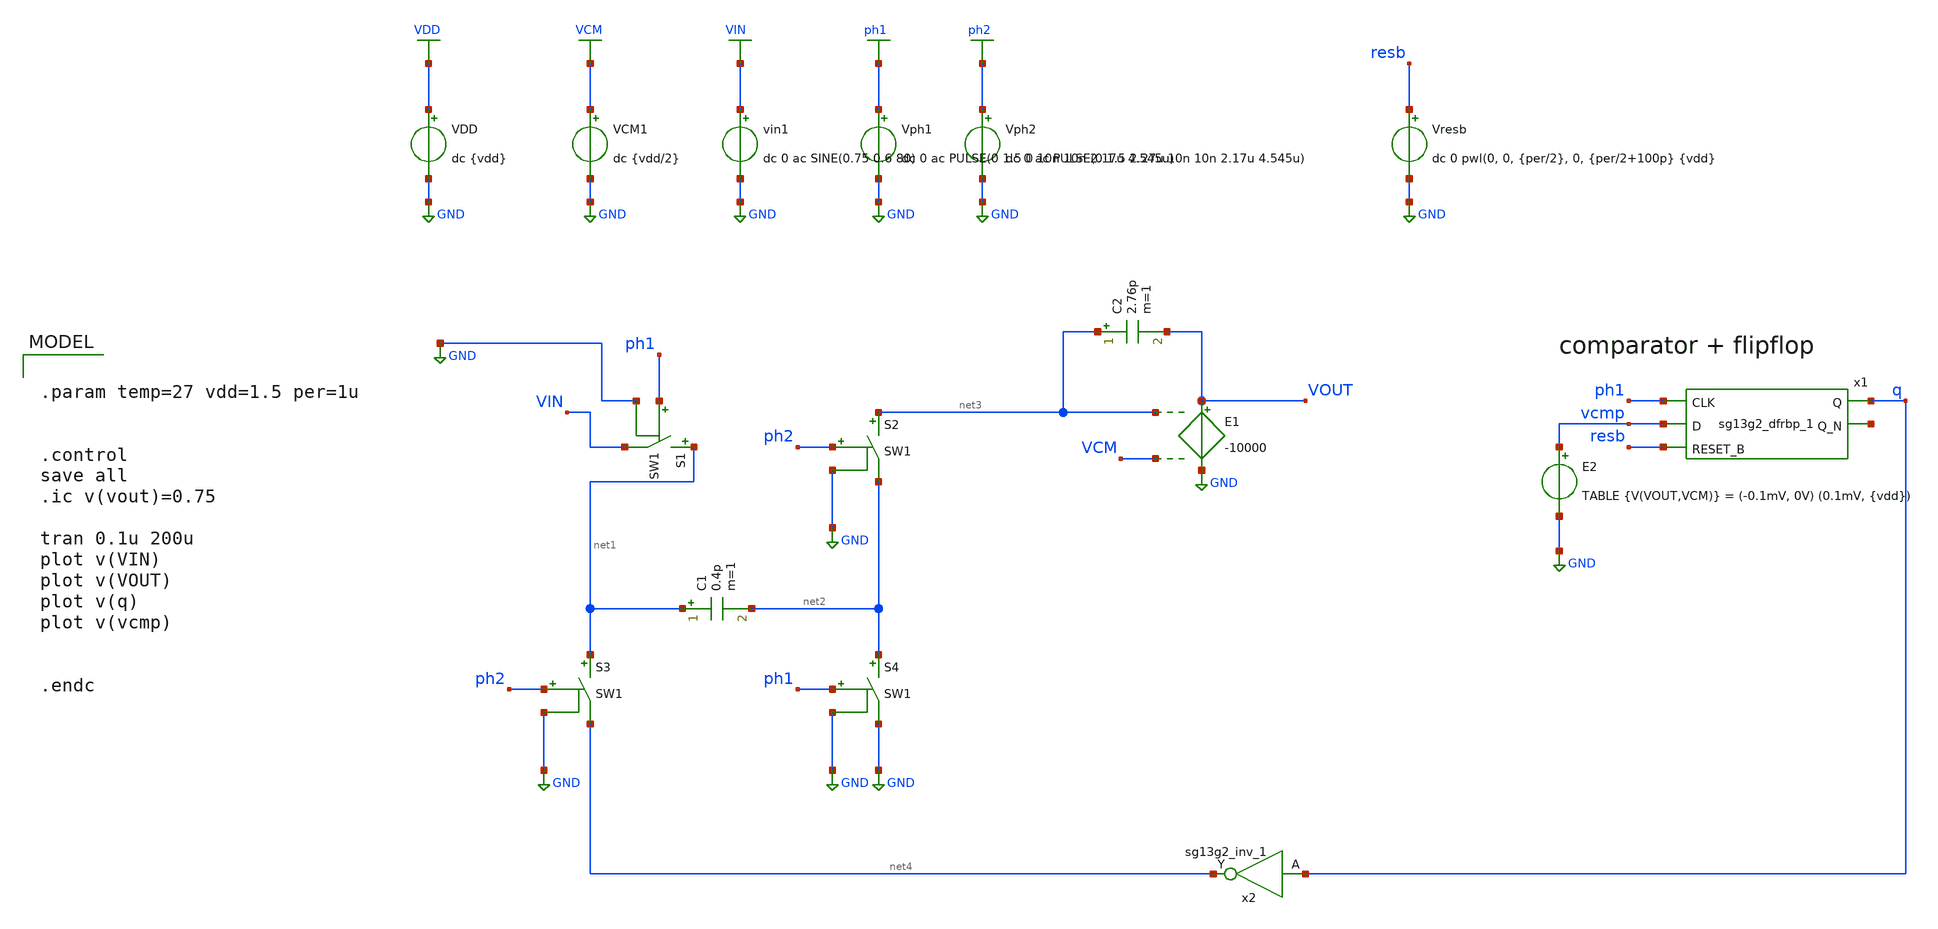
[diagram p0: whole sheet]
** sch_path: DSM_1storder/Schematic_Level/xschem/ideal_schematics/untitled.sch
**.subckt untitled
C1 net1 net2 0.4p m=1
S1 net1 VIN ph1 GND SW1
S2 net3 net2 ph2 GND SW1
S3 net1 net4 ph2 GND SW1
S4 net2 GND ph1 GND SW1
VDD VDD GND dc {vdd}
VCM1 VCM GND dc {vdd/2}
vin1 VIN GND dc 0 ac SINE(0.75 0.6 80)
Vph2 ph2 GND dc 0 ac PULSE(0 1.5 2.27u 10n 10n 2.17u 4.545u)
Vph1 ph1 GND dc 0 ac PULSE(0 1.5 0 10n 10n 2.17u 4.545u)
E1 VOUT GND net3 VCM -10000
C2 net3 VOUT 2.76p m=1
E2 vcmp GND TABLE {V(VOUT,VCM)} = (-0.1mV, 0V) (0.1mV, {vdd})
x1 q net5 ph1 vcmp resb VDD VSS sg13g2_dfrbp_1
Vresb resb GND dc 0 pwl(0, 0, {per/2}, 0, {per/2+100p} {vdd}
x2 net4 q 1.5 0 sg13g2_inv_1
**** begin user architecture code


.param temp=27 vdd=1.5 per=1u


.control
save all
.ic v(vout)=0.75

tran 0.1u 200u
plot v(VIN)
plot v(VOUT)
plot v(q)
plot v(vcmp)


.endc



.lib $::SG13G2_MODELS/cornerMOSlv.lib mos_tt
.lib $::SG13G2_MODELS/cornerRES.lib res_typ
.inc /foss/pdks/ihp-sg13g2/libs.ref/sg13g2_stdcell/spice/sg13g2_stdcell.spice

**** end user architecture code
**.ends

* expanding   symbol:  sg13g2_stdcells/sg13g2_dfrbp_1.sym # of pins=5
** sym_path: sg13g2_stdcells/sg13g2_dfrbp_1.sym
** sch_path: sg13g2_stdcells/sg13g2_dfrbp_1.sch
.subckt sg13g2_dfrbp_1 Q Q_N CLK D RESET_B VDD VSS
*.ipin D
*.ipin RESET_B
*.ipin CLK
*.opin Q
*.opin Q_N
*.iopin VDD
*.iopin VSS
XM1 Db D net10 VSS sg13_lv_nmos w=420.00n l=130.00n ng=1 m=1 mm_ok=1
XM2 net10 RESET_B VSS VSS sg13_lv_nmos w=420.00n l=130.00n ng=1 m=1 mm_ok=1
XM3 net1 clkneg net9 VSS sg13_lv_nmos w=420.00n l=130.00n ng=1 m=1 mm_ok=1
XM4 net9 net1 VSS VSS sg13_lv_nmos w=420.00n l=130.00n ng=1 m=1 mm_ok=1
XM5 net1 net1 net5 VSS sg13_lv_nmos w=420.00n l=130.00n ng=1 m=1 mm_ok=1
XM6 net5 RESET_B VSS VSS sg13_lv_nmos w=420.00n l=130.00n ng=1 m=1 mm_ok=1
XM7 Q_N net1 VSS VSS sg13_lv_nmos w=740.00n l=130.00n ng=1 m=1 mm_ok=1
XM8 net2 net1 VSS VSS sg13_lv_nmos w=740.00n l=130.00n ng=1 m=1 mm_ok=1
XM9 Q net2 VSS VSS sg13_lv_nmos w=740.00n l=130.00n ng=1 m=1 mm_ok=1
XM10 clkneg CLK VSS VSS sg13_lv_nmos w=740.00n l=130.00n ng=1 m=1 mm_ok=1
XM11 clkpos clkneg VSS VSS sg13_lv_nmos w=740.00n l=130.00n ng=1 m=1 mm_ok=1
XM12 Db clkneg net3 VSS sg13_lv_nmos w=420.00n l=130.00n ng=1 m=1 mm_ok=1
XM13 net3 clkpos net8 VSS sg13_lv_nmos w=420.00n l=130.00n ng=1 m=1 mm_ok=1
XM14 net8 net3 net4 VSS sg13_lv_nmos w=420.00n l=130.00n ng=1 m=1 mm_ok=1
XM15 net4 RESET_B VSS VSS sg13_lv_nmos w=420.00n l=130.00n ng=1 m=1 mm_ok=1
XM16 net3 net3 VSS VSS sg13_lv_nmos w=740.00n l=130.00n ng=1 m=1 mm_ok=1
XM17 net3 clkpos net1 VSS sg13_lv_nmos w=740.00n l=130.00n ng=1 m=1 mm_ok=1
XM18 Db RESET_B VDD VDD sg13_lv_pmos w=420.00n l=130.00n ng=1 m=1 mm_ok=1
XM19 Db D VDD VDD sg13_lv_pmos w=420.00n l=130.00n ng=1 m=1 mm_ok=1
XM20 net7 net1 VDD VDD sg13_lv_pmos w=420.00n l=130.00n ng=1 m=1 mm_ok=1
XM21 net1 clkpos net7 VDD sg13_lv_pmos w=420.00n l=130.00n ng=1 m=1 mm_ok=1
XM22 net1 net1 VDD VDD sg13_lv_pmos w=420.00n l=130.00n ng=1 m=1 mm_ok=1
XM23 net1 RESET_B VDD VDD sg13_lv_pmos w=420.00n l=130.00n ng=1 m=1 mm_ok=1
XM24 Q_N net1 VDD VDD sg13_lv_pmos w=1.12u l=130.00n ng=1 m=1 mm_ok=1
XM25 net2 net1 VDD VDD sg13_lv_pmos w=1.12u l=130.00n ng=1 m=1 mm_ok=1
XM26 Q net2 VDD VDD sg13_lv_pmos w=1.12u l=130.00n ng=1 m=1 mm_ok=1
XM27 clkneg CLK VDD VDD sg13_lv_pmos w=1.12u l=130.00n ng=1 m=1 mm_ok=1
XM28 clkpos clkneg VDD VDD sg13_lv_pmos w=1.12u l=130.00n ng=1 m=1 mm_ok=1
XM29 Db clkpos net3 VDD sg13_lv_pmos w=420.00n l=130.00n ng=1 m=1 mm_ok=1
XM30 net6 net3 VDD VDD sg13_lv_pmos w=420.00n l=130.00n ng=1 m=1 mm_ok=1
XM31 net3 clkneg net6 VDD sg13_lv_pmos w=420.00n l=130.00n ng=1 m=1 mm_ok=1
XM32 net3 RESET_B VDD VDD sg13_lv_pmos w=420.00n l=130.00n ng=1 m=1 mm_ok=1
XM33 net3 net3 VDD VDD sg13_lv_pmos w=1.000u l=130.00n ng=1 m=1 mm_ok=1
XM34 net3 clkneg net1 VDD sg13_lv_pmos w=1.000u l=130.00n ng=1 m=1 mm_ok=1
.ends


* expanding   symbol:  sg13g2_stdcells/sg13g2_inv_1.sym # of pins=2
** sym_path: sg13g2_stdcells/sg13g2_inv_1.sym
** sch_path: sg13g2_stdcells/sg13g2_inv_1.sch
.subckt sg13g2_inv_1 Y A VDD VSS
*.opin Y
*.ipin A
*.iopin VDD
*.iopin VSS
XM1 Y A VSS VSS sg13_lv_nmos w=740.00n l=130.00n ng=1 m=1 mm_ok=1
XM2 Y A VDD VDD sg13_lv_pmos w=1.12u l=130.00n ng=1 m=1 mm_ok=1
.ends

.GLOBAL GND
.GLOBAL VDD
.GLOBAL VCM
.GLOBAL VIN
.GLOBAL ph2
.GLOBAL ph1
**** begin user architecture code
.MODEL SW1 SW   VT=0.75 VH=0.01  RON=10 ROFF=10G
**** end user architecture code
.end
